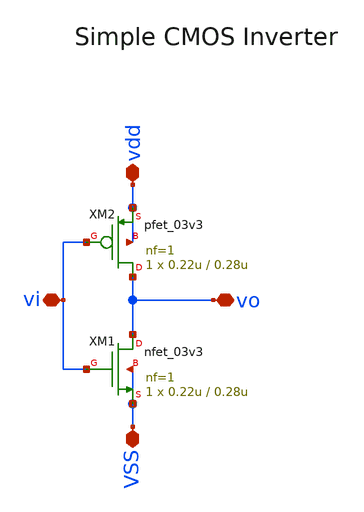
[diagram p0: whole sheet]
** sch_path: designs/inv.sch
**.subckt inv vdd VSS vi vo
*.iopin vdd
*.iopin VSS
*.iopin vi
*.iopin vo
XM1 vo vi VSS VSS nfet_03v3 L=0.28u W=0.22u nf=1 ad='int((nf+1)/2) * W/nf * 0.18u' as='int((nf+2)/2) * W/nf * 0.18u'
+ pd='2*int((nf+1)/2) * (W/nf + 0.18u)' ps='2*int((nf+2)/2) * (W/nf + 0.18u)' nrd='0.18u / W' nrs='0.18u / W'
+ sa=0 sb=0 sd=0 m=1
XM2 vo vi vdd vdd pfet_03v3 L=0.28u W=0.22u nf=1 ad='int((nf+1)/2) * W/nf * 0.18u' as='int((nf+2)/2) * W/nf * 0.18u'
+ pd='2*int((nf+1)/2) * (W/nf + 0.18u)' ps='2*int((nf+2)/2) * (W/nf + 0.18u)' nrd='0.18u / W' nrs='0.18u / W'
+ sa=0 sb=0 sd=0 m=1
**.ends
.end
